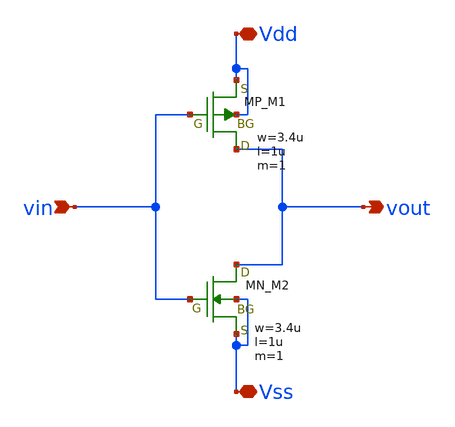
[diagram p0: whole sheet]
** sch_path: member_project/inverter/sanken/exodjp/inverter_exodjp.sch
**.subckt inverter_exodjp Vdd Vss vin vout
*.iopin Vdd
*.iopin Vss
*.ipin vin
*.opin vout
XM1 vout vin Vdd Vdd PMOS w=3.4u l=1u as=0 ad=0 ps=0 pd=0 nrd=0 nrs=0 m=1
XM2 vout vin Vss Vss NMOS w=3.4u l=1u as=0 ad=0 ps=0 pd=0 nrd=0 nrs=0 m=1
**.ends
.end
